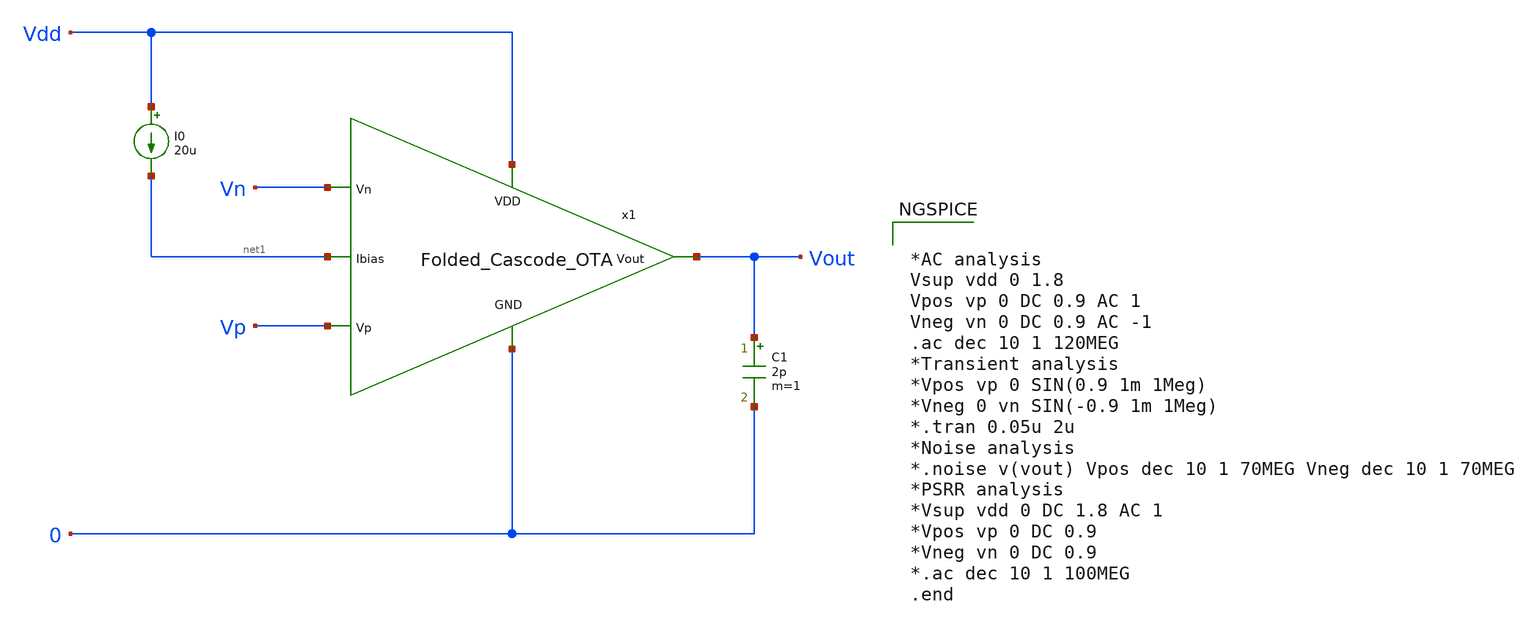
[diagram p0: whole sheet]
** sch_path: Analog_Blocks/OTA/Testbench/Folded_Cscode_OTA_TB.sch
**.subckt Folded_Cscode_OTA_TB
I0 Vdd net1 20u
C1 Vout 0 2p m=1
x1 Vdd Vout Vp Vn net1 0 Folded_Cascode_OTA
**** begin user architecture code

.include $::SKYWATER_MODELS/cells/nfet_01v8/sky130_fd_pr__nfet_01v8__tt.corner.spice
.include $::SKYWATER_MODELS/cells/nfet_01v8_lvt/sky130_fd_pr__nfet_01v8_lvt__tt.corner.spice
.include $::SKYWATER_MODELS/cells/pfet_01v8/sky130_fd_pr__pfet_01v8__tt.corner.spice
.include $::SKYWATER_MODELS/cells/nfet_03v3_nvt/sky130_fd_pr__nfet_03v3_nvt__tt.corner.spice
.include $::SKYWATER_MODELS/cells/nfet_05v0_nvt/sky130_fd_pr__nfet_05v0_nvt__tt.corner.spice
.include $::SKYWATER_MODELS/cells/esd_nfet_01v8/sky130_fd_pr__esd_nfet_01v8__tt.corner.spice
.include $::SKYWATER_MODELS/cells/pfet_01v8_lvt/sky130_fd_pr__pfet_01v8_lvt__tt.corner.spice
.include $::SKYWATER_MODELS/cells/pfet_01v8_hvt/sky130_fd_pr__pfet_01v8_hvt__tt.corner.spice
.include $::SKYWATER_MODELS/cells/esd_pfet_g5v0d10v5/sky130_fd_pr__esd_pfet_g5v0d10v5__tt.corner.spice
.include $::SKYWATER_MODELS/cells/pfet_g5v0d10v5/sky130_fd_pr__pfet_g5v0d10v5__tt.corner.spice
.include $::SKYWATER_MODELS/cells/pfet_g5v0d16v0/sky130_fd_pr__pfet_g5v0d16v0__tt.corner.spice
.include $::SKYWATER_MODELS/cells/nfet_g5v0d10v5/sky130_fd_pr__nfet_g5v0d10v5__tt.corner.spice
.include $::SKYWATER_MODELS/cells/nfet_g5v0d16v0/sky130_fd_pr__nfet_g5v0d16v0__tt_discrete.corner.spice
.include $::SKYWATER_MODELS/cells/esd_nfet_g5v0d10v5/sky130_fd_pr__esd_nfet_g5v0d10v5__tt.corner.spice
.include $::SKYWATER_MODELS/models/corners/tt/nonfet.spice
* Mismatch parameters
.include $::SKYWATER_MODELS/cells/nfet_01v8/sky130_fd_pr__nfet_01v8__mismatch.corner.spice
.include $::SKYWATER_MODELS/cells/pfet_01v8/sky130_fd_pr__pfet_01v8__mismatch.corner.spice
.include $::SKYWATER_MODELS/cells/nfet_01v8_lvt/sky130_fd_pr__nfet_01v8_lvt__mismatch.corner.spice
.include $::SKYWATER_MODELS/cells/pfet_01v8_lvt/sky130_fd_pr__pfet_01v8_lvt__mismatch.corner.spice
.include $::SKYWATER_MODELS/cells/pfet_01v8_hvt/sky130_fd_pr__pfet_01v8_hvt__mismatch.corner.spice
.include $::SKYWATER_MODELS/cells/nfet_g5v0d10v5/sky130_fd_pr__nfet_g5v0d10v5__mismatch.corner.spice
.include $::SKYWATER_MODELS/cells/pfet_g5v0d10v5/sky130_fd_pr__pfet_g5v0d10v5__mismatch.corner.spice
.include $::SKYWATER_MODELS/cells/nfet_05v0_nvt/sky130_fd_pr__nfet_05v0_nvt__mismatch.corner.spice
.include $::SKYWATER_MODELS/cells/nfet_03v3_nvt/sky130_fd_pr__nfet_03v3_nvt__mismatch.corner.spice
* Resistor$::SKYWATER_MODELS/Capacitor
.include $::SKYWATER_MODELS/models/r+c/res_typical__cap_typical.spice
.include $::SKYWATER_MODELS/models/r+c/res_typical__cap_typical__lin.spice
* Special cells
.include $::SKYWATER_MODELS/models/corners/tt/specialized_cells.spice
* All models
.include $::SKYWATER_MODELS/models/all.spice
* Corner
.include $::SKYWATER_MODELS/models/corners/tt/rf.spice



*AC analysis
Vsup vdd 0 1.8
Vpos vp 0 DC 0.9 AC 1
Vneg vn 0 DC 0.9 AC -1
.ac dec 10 1 120MEG
*Transient analysis
*Vpos vp 0 SIN(0.9 1m 1Meg)
*Vneg 0 vn SIN(-0.9 1m 1Meg)
*.tran 0.05u 2u
*Noise analysis
*.noise v(vout) Vpos dec 10 1 70MEG Vneg dec 10 1 70MEG
*PSRR analysis
*Vsup vdd 0 DC 1.8 AC 1
*Vpos vp 0 DC 0.9
*Vneg vn 0 DC 0.9
*.ac dec 10 1 100MEG
.end


**** end user architecture code
**.ends
.end
